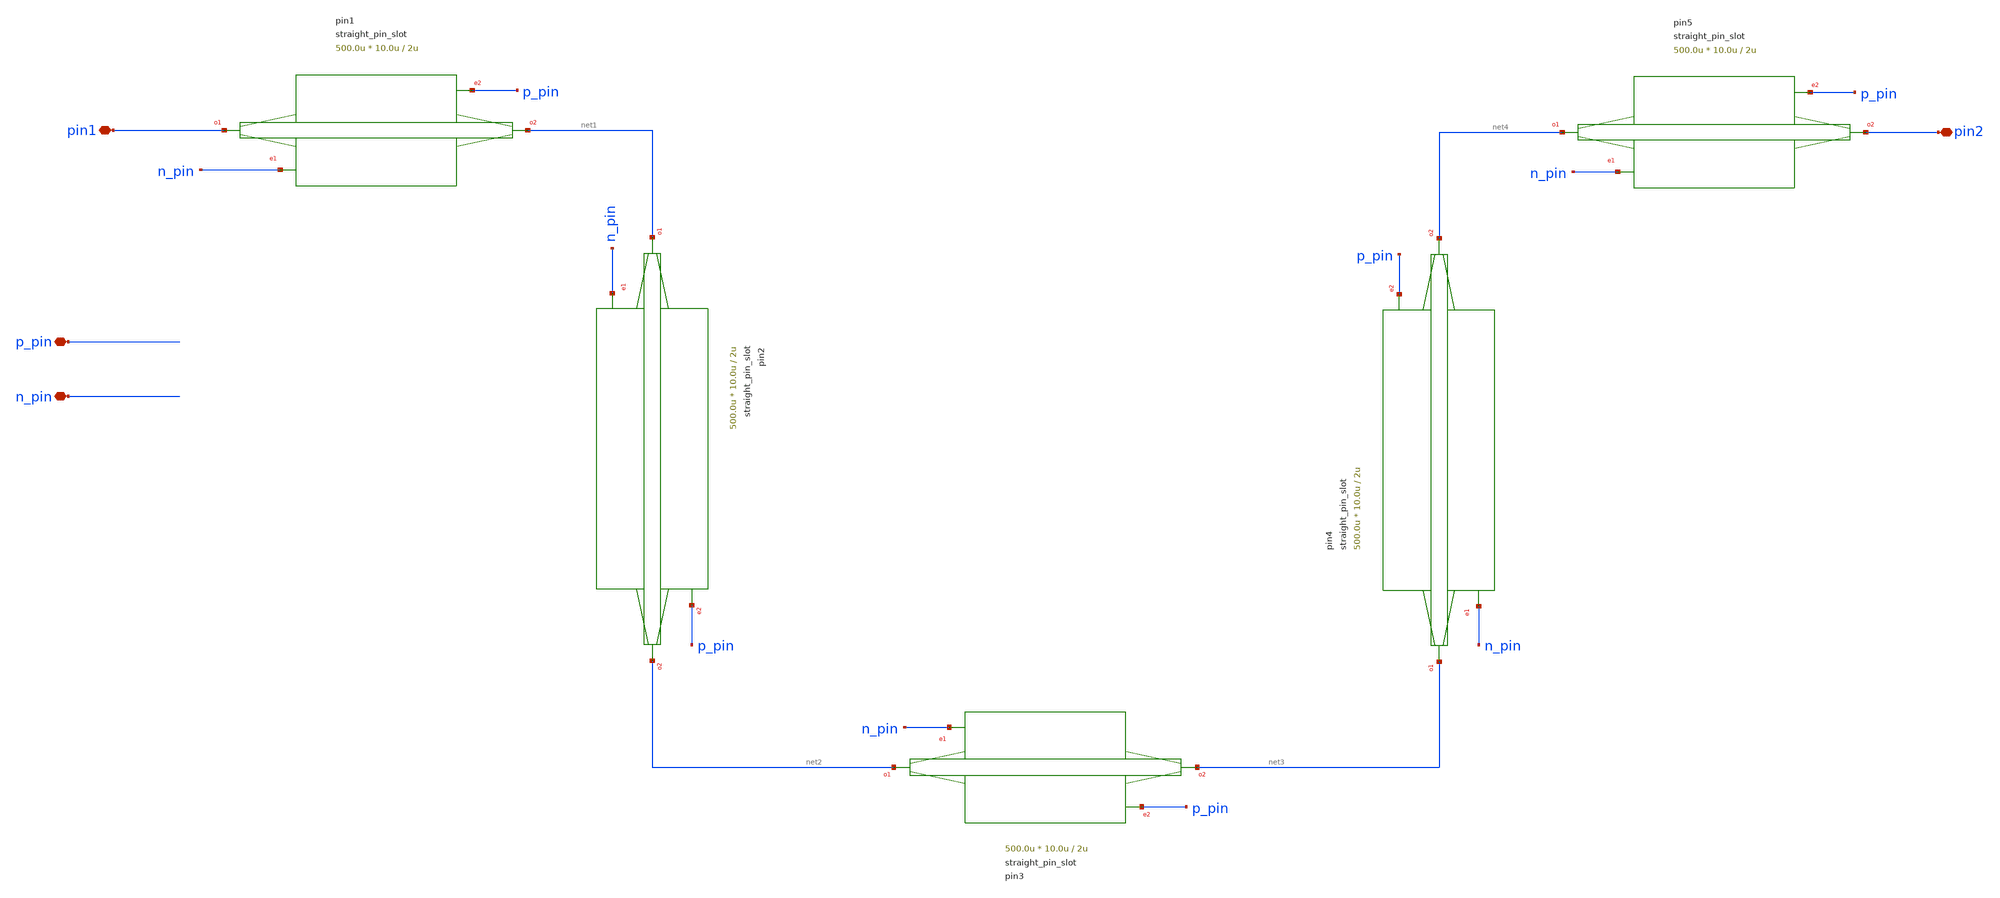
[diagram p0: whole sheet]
** sch_path: xschem/tests/test_sch/test_straight_pin_slot.sch
* Copyright (c) 2024, Mabrains LLC
* Licensed under the GNU Lesser General Public License, Version 3.0 (the "License");
* you may not use this file except in compliance with the License.
* GNU Lesser General Public License
* Version 3, 29 June 2007
* This program is free software: you can redistribute it and/or modify
* it under the terms of the GNU Lesser General Public License as published
* by the Free Software Foundation, either version 3 of the License, or
* (at your option) any later version.
* This program is distributed in the hope that it will be useful,
* but WITHOUT ANY WARRANTY; without even the implied warranty of
* MERCHANTABILITY or FITNESS FOR A PARTICULAR PURPOSE.  See the
* GNU Lesser General Public License for more details.
* You should have received a copy of the GNU Lesser General Public License
* along with this program.  If not, see <https://www.gnu.org/licenses/>.
* SPDX-License-Identifier: LGPL-3.0
**.subckt test_straight_pin_slot pin1 pin2 p_pin n_pin
*.iopin pin1
*.iopin pin2
*.iopin p_pin
*.iopin n_pin
Ppin1 pin1 net1 n_pin p_pin straight_pin_slot length=500.0u via_stack_width=10.0u
+ via_stack_slab_width=10.0u via_stack_spacing=2u via_stack_slab_spacing=2.0u
Ppin2 net1 net2 n_pin p_pin straight_pin_slot length=500.0u via_stack_width=10.0u
+ via_stack_slab_width=10.0u via_stack_spacing=2u via_stack_slab_spacing=2.0u
Ppin3 net2 net3 n_pin p_pin straight_pin_slot length=500.0u via_stack_width=10.0u
+ via_stack_slab_width=10.0u via_stack_spacing=2u via_stack_slab_spacing=2.0u
Ppin4 net3 net4 n_pin p_pin straight_pin_slot length=500.0u via_stack_width=10.0u
+ via_stack_slab_width=10.0u via_stack_spacing=2u via_stack_slab_spacing=2.0u
Ppin5 net4 pin2 n_pin p_pin straight_pin_slot length=500.0u via_stack_width=10.0u
+ via_stack_slab_width=10.0u via_stack_spacing=2u via_stack_slab_spacing=2.0u
**.ends
.end
